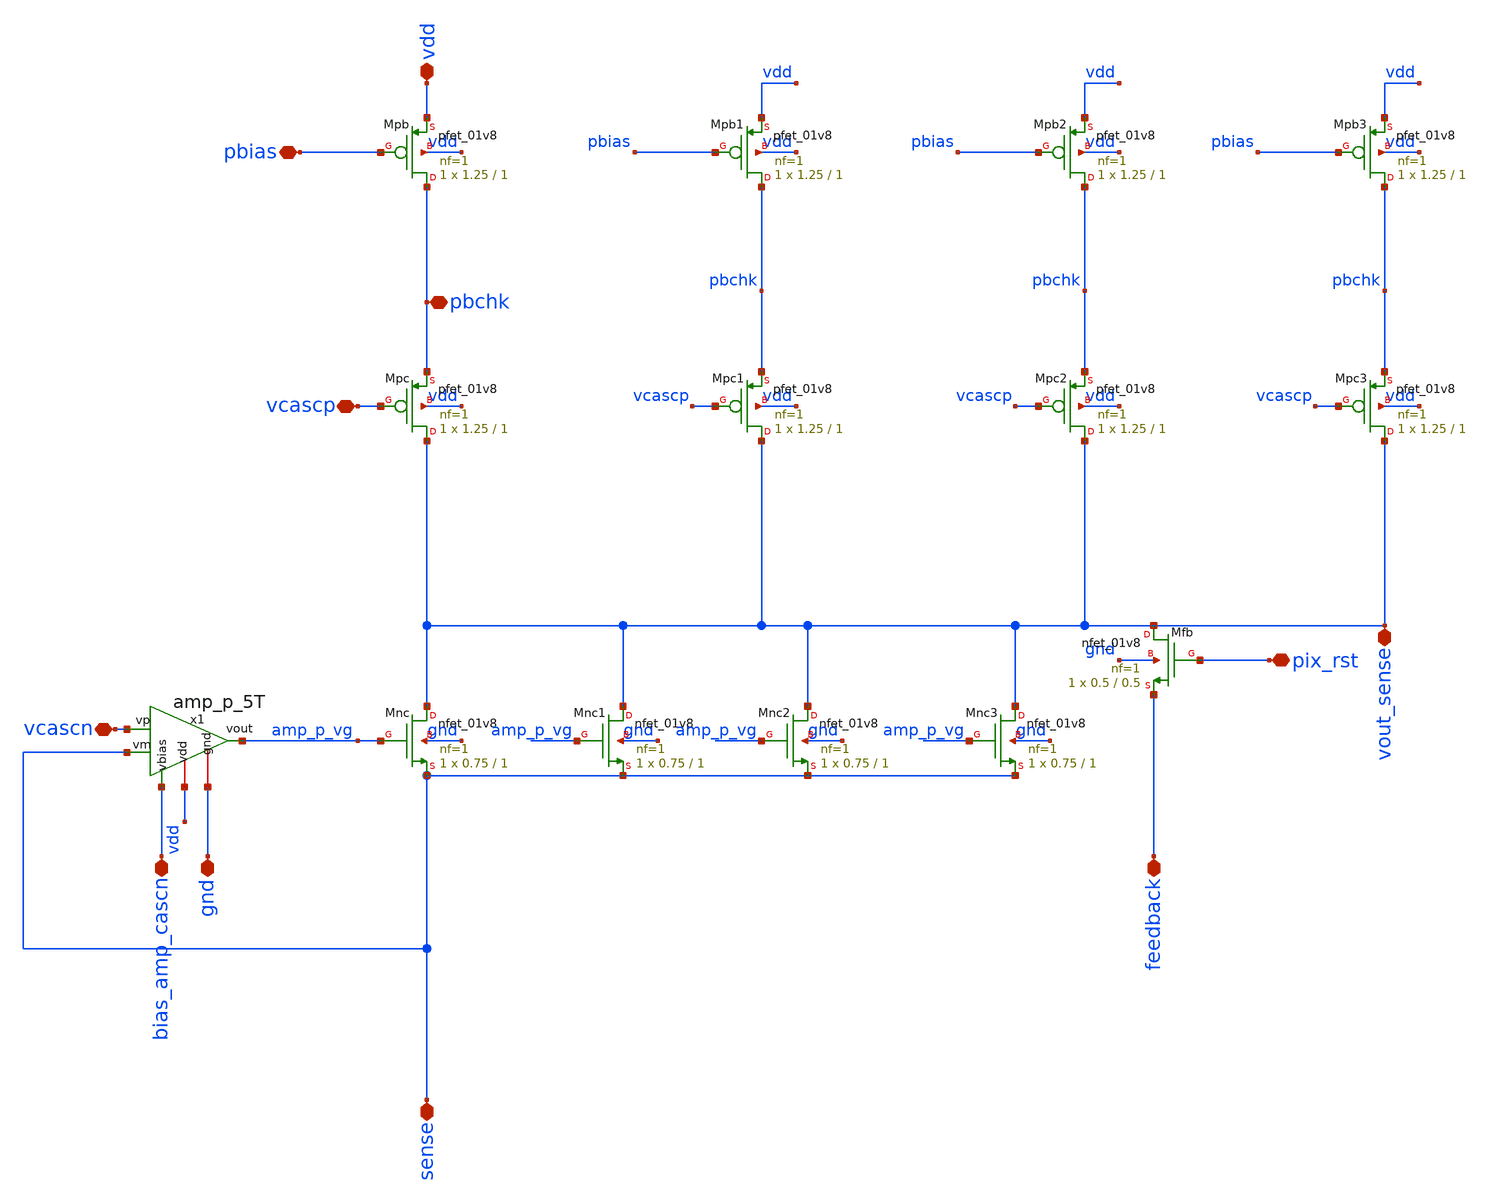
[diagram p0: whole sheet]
** sch_path: analog/xschem/col_amp_n_clamp_v1/col_amp_v1.sch
**.subckt col_amp_v1 vdd gnd sense vout_sense feedback pbchk pix_rst vcascn vcascp pbias
*+ bias_amp_cascn
*.iopin vdd
*.iopin gnd
*.iopin sense
*.iopin vout_sense
*.iopin feedback
*.iopin pbchk
*.iopin pix_rst
*.iopin vcascn
*.iopin vcascp
*.iopin pbias
*.iopin bias_amp_cascn
XMpb pbchk pbias vdd vdd sky130_fd_pr__pfet_01v8 L=1 W=1.25 nf=1 ad='int((1 + 1)/2) * 1.25 / 1 * 0.29'
+ as='int((1 + 2)/2) * 1.25 / 1 * 0.29' pd='2*int((1 + 1)/2) * (1.25 / 1 + 0.29)' ps='2*int((1 + 2)/2) * (1.25 / 1 + 0.29)'
+ nrd='0.29 / 1.25 ' nrs='0.29 / 1.25 ' sa=0 sb=0 sd=0 mult=1 m=1
XMnc vout_sense amp_p_vg sense gnd sky130_fd_pr__nfet_01v8 L=1 W=0.75 nf=1 ad='int((1 + 1)/2) * 0.75 / 1 * 0.29'
+ as='int((1 + 2)/2) * 0.75 / 1 * 0.29' pd='2*int((1 + 1)/2) * (0.75 / 1 + 0.29)' ps='2*int((1 + 2)/2) * (0.75 / 1 + 0.29)'
+ nrd='0.29 / 0.75 ' nrs='0.29 / 0.75 ' sa=0 sb=0 sd=0 mult=1 m=1
XMfb vout_sense pix_rst feedback gnd sky130_fd_pr__nfet_01v8 L=0.5 W=0.5 nf=1 ad='int((1 + 1)/2) * 0.5 / 1 * 0.29'
+ as='int((1 + 2)/2) * 0.5 / 1 * 0.29' pd='2*int((1 + 1)/2) * (0.5 / 1 + 0.29)' ps='2*int((1 + 2)/2) * (0.5 / 1 + 0.29)'
+ nrd='0.29 / 0.5 ' nrs='0.29 / 0.5 ' sa=0 sb=0 sd=0 mult=1 m=1
XMpc vout_sense vcascp pbchk vdd sky130_fd_pr__pfet_01v8 L=1 W=1.25 nf=1 ad='int((1 + 1)/2) * 1.25 / 1 * 0.29'
+ as='int((1 + 2)/2) * 1.25 / 1 * 0.29' pd='2*int((1 + 1)/2) * (1.25 / 1 + 0.29)' ps='2*int((1 + 2)/2) * (1.25 / 1 + 0.29)'
+ nrd='0.29 / 1.25 ' nrs='0.29 / 1.25 ' sa=0 sb=0 sd=0 mult=1 m=1
XMpb1 pbchk pbias vdd vdd sky130_fd_pr__pfet_01v8 L=1 W=1.25 nf=1 ad='int((1 + 1)/2) * 1.25 / 1 * 0.29'
+ as='int((1 + 2)/2) * 1.25 / 1 * 0.29' pd='2*int((1 + 1)/2) * (1.25 / 1 + 0.29)' ps='2*int((1 + 2)/2) * (1.25 / 1 + 0.29)'
+ nrd='0.29 / 1.25 ' nrs='0.29 / 1.25 ' sa=0 sb=0 sd=0 mult=1 m=1
XMpc1 vout_sense vcascp pbchk vdd sky130_fd_pr__pfet_01v8 L=1 W=1.25 nf=1 ad='int((1 + 1)/2) * 1.25 / 1 * 0.29'
+ as='int((1 + 2)/2) * 1.25 / 1 * 0.29' pd='2*int((1 + 1)/2) * (1.25 / 1 + 0.29)' ps='2*int((1 + 2)/2) * (1.25 / 1 + 0.29)'
+ nrd='0.29 / 1.25 ' nrs='0.29 / 1.25 ' sa=0 sb=0 sd=0 mult=1 m=1
XMpb2 pbchk pbias vdd vdd sky130_fd_pr__pfet_01v8 L=1 W=1.25 nf=1 ad='int((1 + 1)/2) * 1.25 / 1 * 0.29'
+ as='int((1 + 2)/2) * 1.25 / 1 * 0.29' pd='2*int((1 + 1)/2) * (1.25 / 1 + 0.29)' ps='2*int((1 + 2)/2) * (1.25 / 1 + 0.29)'
+ nrd='0.29 / 1.25 ' nrs='0.29 / 1.25 ' sa=0 sb=0 sd=0 mult=1 m=1
XMpc2 vout_sense vcascp pbchk vdd sky130_fd_pr__pfet_01v8 L=1 W=1.25 nf=1 ad='int((1 + 1)/2) * 1.25 / 1 * 0.29'
+ as='int((1 + 2)/2) * 1.25 / 1 * 0.29' pd='2*int((1 + 1)/2) * (1.25 / 1 + 0.29)' ps='2*int((1 + 2)/2) * (1.25 / 1 + 0.29)'
+ nrd='0.29 / 1.25 ' nrs='0.29 / 1.25 ' sa=0 sb=0 sd=0 mult=1 m=1
XMpb3 pbchk pbias vdd vdd sky130_fd_pr__pfet_01v8 L=1 W=1.25 nf=1 ad='int((1 + 1)/2) * 1.25 / 1 * 0.29'
+ as='int((1 + 2)/2) * 1.25 / 1 * 0.29' pd='2*int((1 + 1)/2) * (1.25 / 1 + 0.29)' ps='2*int((1 + 2)/2) * (1.25 / 1 + 0.29)'
+ nrd='0.29 / 1.25 ' nrs='0.29 / 1.25 ' sa=0 sb=0 sd=0 mult=1 m=1
XMpc3 vout_sense vcascp pbchk vdd sky130_fd_pr__pfet_01v8 L=1 W=1.25 nf=1 ad='int((1 + 1)/2) * 1.25 / 1 * 0.29'
+ as='int((1 + 2)/2) * 1.25 / 1 * 0.29' pd='2*int((1 + 1)/2) * (1.25 / 1 + 0.29)' ps='2*int((1 + 2)/2) * (1.25 / 1 + 0.29)'
+ nrd='0.29 / 1.25 ' nrs='0.29 / 1.25 ' sa=0 sb=0 sd=0 mult=1 m=1
XMnc1 vout_sense amp_p_vg sense gnd sky130_fd_pr__nfet_01v8 L=1 W=0.75 nf=1 ad='int((1 + 1)/2) * 0.75 / 1 * 0.29'
+ as='int((1 + 2)/2) * 0.75 / 1 * 0.29' pd='2*int((1 + 1)/2) * (0.75 / 1 + 0.29)' ps='2*int((1 + 2)/2) * (0.75 / 1 + 0.29)'
+ nrd='0.29 / 0.75 ' nrs='0.29 / 0.75 ' sa=0 sb=0 sd=0 mult=1 m=1
XMnc2 vout_sense amp_p_vg sense gnd sky130_fd_pr__nfet_01v8 L=1 W=0.75 nf=1 ad='int((1 + 1)/2) * 0.75 / 1 * 0.29'
+ as='int((1 + 2)/2) * 0.75 / 1 * 0.29' pd='2*int((1 + 1)/2) * (0.75 / 1 + 0.29)' ps='2*int((1 + 2)/2) * (0.75 / 1 + 0.29)'
+ nrd='0.29 / 0.75 ' nrs='0.29 / 0.75 ' sa=0 sb=0 sd=0 mult=1 m=1
XMnc3 vout_sense amp_p_vg sense gnd sky130_fd_pr__nfet_01v8 L=1 W=0.75 nf=1 ad='int((1 + 1)/2) * 0.75 / 1 * 0.29'
+ as='int((1 + 2)/2) * 0.75 / 1 * 0.29' pd='2*int((1 + 1)/2) * (0.75 / 1 + 0.29)' ps='2*int((1 + 2)/2) * (0.75 / 1 + 0.29)'
+ nrd='0.29 / 0.75 ' nrs='0.29 / 0.75 ' sa=0 sb=0 sd=0 mult=1 m=1
x1 vdd amp_p_vg vcascn sense bias_amp_cascn gnd amp_p_5T
**.ends

* expanding   symbol:
*+  /home/user/projects/nic2025_v2/nic2025_openDVS/analog/xschem/final/col_amp_n_clamp_v1/amp_p_5T.sym # of pins=6
** sym_path: analog/xschem/final/col_amp_n_clamp_v1/amp_p_5T.sym
** sch_path: analog/xschem/final/col_amp_n_clamp_v1/amp_p_5T.sch
.subckt amp_p_5T vdd vout vp vm vbias gnd
*.iopin gnd
*.iopin vdd
*.iopin vout
*.iopin vbias
*.iopin vm
*.iopin vp
XMinm vout vm vsource vdd sky130_fd_pr__pfet_01v8 L=0.2 W=0.5 nf=1 ad='int((1 + 1)/2) * 0.5 / 1 * 0.29'
+ as='int((1 + 2)/2) * 0.5 / 1 * 0.29' pd='2*int((1 + 1)/2) * (0.5 / 1 + 0.29)' ps='2*int((1 + 2)/2) * (0.5 / 1 + 0.29)'
+ nrd='0.29 / 0.5 ' nrs='0.29 / 0.5 ' sa=0 sb=0 sd=0 mult=1 m=1
XMinp vdio vp vsource vdd sky130_fd_pr__pfet_01v8 L=0.2 W=0.5 nf=1 ad='int((1 + 1)/2) * 0.5 / 1 * 0.29'
+ as='int((1 + 2)/2) * 0.5 / 1 * 0.29' pd='2*int((1 + 1)/2) * (0.5 / 1 + 0.29)' ps='2*int((1 + 2)/2) * (0.5 / 1 + 0.29)'
+ nrd='0.29 / 0.5 ' nrs='0.29 / 0.5 ' sa=0 sb=0 sd=0 mult=1 m=1
XMdio vdio vdio gnd gnd sky130_fd_pr__nfet_01v8 L=0.2 W=0.5 nf=1 ad='int((1 + 1)/2) * 0.5 / 1 * 0.29'
+ as='int((1 + 2)/2) * 0.5 / 1 * 0.29' pd='2*int((1 + 1)/2) * (0.5 / 1 + 0.29)' ps='2*int((1 + 2)/2) * (0.5 / 1 + 0.29)'
+ nrd='0.29 / 0.5 ' nrs='0.29 / 0.5 ' sa=0 sb=0 sd=0 mult=1 m=1
XMmirr vout vdio gnd gnd sky130_fd_pr__nfet_01v8 L=0.2 W=0.5 nf=1 ad='int((1 + 1)/2) * 0.5 / 1 * 0.29'
+ as='int((1 + 2)/2) * 0.5 / 1 * 0.29' pd='2*int((1 + 1)/2) * (0.5 / 1 + 0.29)' ps='2*int((1 + 2)/2) * (0.5 / 1 + 0.29)'
+ nrd='0.29 / 0.5 ' nrs='0.29 / 0.5 ' sa=0 sb=0 sd=0 mult=1 m=1
XMbias vsource vbias vdd vdd sky130_fd_pr__pfet_01v8 L=1 W=0.5 nf=1 ad='int((1 + 1)/2) * 0.5 / 1 * 0.29'
+ as='int((1 + 2)/2) * 0.5 / 1 * 0.29' pd='2*int((1 + 1)/2) * (0.5 / 1 + 0.29)' ps='2*int((1 + 2)/2) * (0.5 / 1 + 0.29)'
+ nrd='0.29 / 0.5 ' nrs='0.29 / 0.5 ' sa=0 sb=0 sd=0 mult=1 m=1
XMbias1 vsource vbias vdd vdd sky130_fd_pr__pfet_01v8 L=1 W=0.5 nf=1 ad='int((1 + 1)/2) * 0.5 / 1 * 0.29'
+ as='int((1 + 2)/2) * 0.5 / 1 * 0.29' pd='2*int((1 + 1)/2) * (0.5 / 1 + 0.29)' ps='2*int((1 + 2)/2) * (0.5 / 1 + 0.29)'
+ nrd='0.29 / 0.5 ' nrs='0.29 / 0.5 ' sa=0 sb=0 sd=0 mult=1 m=1
XMbias2 vsource vbias vdd vdd sky130_fd_pr__pfet_01v8 L=1 W=0.5 nf=1 ad='int((1 + 1)/2) * 0.5 / 1 * 0.29'
+ as='int((1 + 2)/2) * 0.5 / 1 * 0.29' pd='2*int((1 + 1)/2) * (0.5 / 1 + 0.29)' ps='2*int((1 + 2)/2) * (0.5 / 1 + 0.29)'
+ nrd='0.29 / 0.5 ' nrs='0.29 / 0.5 ' sa=0 sb=0 sd=0 mult=1 m=1
XMbias3 vsource vbias vdd vdd sky130_fd_pr__pfet_01v8 L=1 W=0.5 nf=1 ad='int((1 + 1)/2) * 0.5 / 1 * 0.29'
+ as='int((1 + 2)/2) * 0.5 / 1 * 0.29' pd='2*int((1 + 1)/2) * (0.5 / 1 + 0.29)' ps='2*int((1 + 2)/2) * (0.5 / 1 + 0.29)'
+ nrd='0.29 / 0.5 ' nrs='0.29 / 0.5 ' sa=0 sb=0 sd=0 mult=1 m=1
XMmirr1 vout vdio gnd gnd sky130_fd_pr__nfet_01v8 L=0.2 W=0.5 nf=1 ad='int((1 + 1)/2) * 0.5 / 1 * 0.29'
+ as='int((1 + 2)/2) * 0.5 / 1 * 0.29' pd='2*int((1 + 1)/2) * (0.5 / 1 + 0.29)' ps='2*int((1 + 2)/2) * (0.5 / 1 + 0.29)'
+ nrd='0.29 / 0.5 ' nrs='0.29 / 0.5 ' sa=0 sb=0 sd=0 mult=1 m=1
XMdio1 vdio vdio gnd gnd sky130_fd_pr__nfet_01v8 L=0.2 W=0.5 nf=1 ad='int((1 + 1)/2) * 0.5 / 1 * 0.29'
+ as='int((1 + 2)/2) * 0.5 / 1 * 0.29' pd='2*int((1 + 1)/2) * (0.5 / 1 + 0.29)' ps='2*int((1 + 2)/2) * (0.5 / 1 + 0.29)'
+ nrd='0.29 / 0.5 ' nrs='0.29 / 0.5 ' sa=0 sb=0 sd=0 mult=1 m=1
XMinm1 vout vm vsource vdd sky130_fd_pr__pfet_01v8 L=0.2 W=0.5 nf=1 ad='int((1 + 1)/2) * 0.5 / 1 * 0.29'
+ as='int((1 + 2)/2) * 0.5 / 1 * 0.29' pd='2*int((1 + 1)/2) * (0.5 / 1 + 0.29)' ps='2*int((1 + 2)/2) * (0.5 / 1 + 0.29)'
+ nrd='0.29 / 0.5 ' nrs='0.29 / 0.5 ' sa=0 sb=0 sd=0 mult=1 m=1
XMinp1 vdio vp vsource vdd sky130_fd_pr__pfet_01v8 L=0.2 W=0.5 nf=1 ad='int((1 + 1)/2) * 0.5 / 1 * 0.29'
+ as='int((1 + 2)/2) * 0.5 / 1 * 0.29' pd='2*int((1 + 1)/2) * (0.5 / 1 + 0.29)' ps='2*int((1 + 2)/2) * (0.5 / 1 + 0.29)'
+ nrd='0.29 / 0.5 ' nrs='0.29 / 0.5 ' sa=0 sb=0 sd=0 mult=1 m=1
.ends

.end
